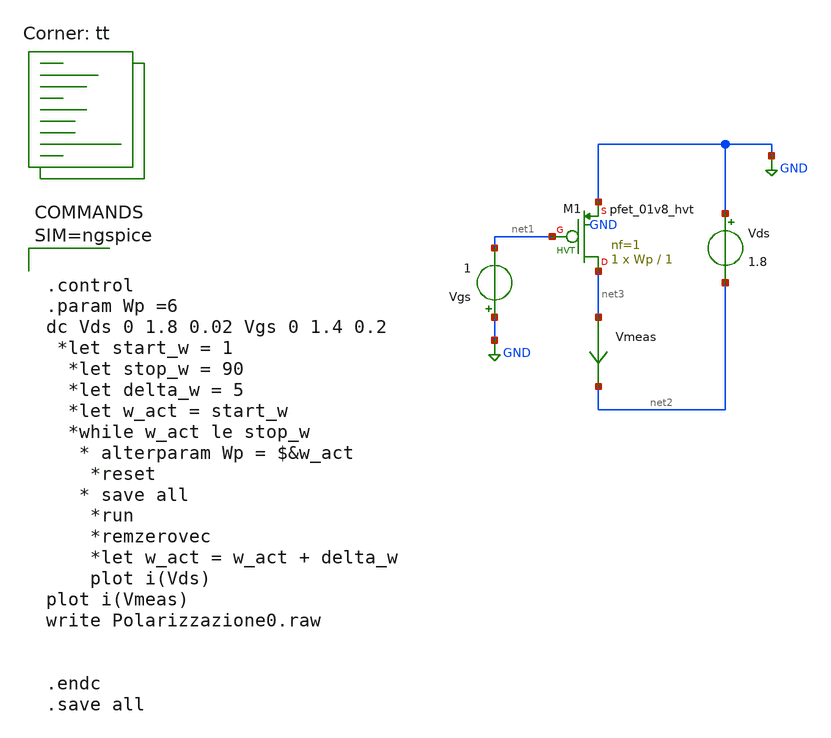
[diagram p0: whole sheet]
** sch_path: xschem/Polarizzazione0.sch
**.subckt Polarizzazione0
Vgs GND net1 1
Vds GND net2 1.8
XM1 net3 net1 GND GND sky130_fd_pr__pfet_01v8_hvt L=1 W=Wp nf=1 ad='int((nf+1)/2) * W/nf * 0.29' as='int((nf+2)/2) * W/nf * 0.29'
+ pd='2*int((nf+1)/2) * (W/nf + 0.29)' ps='2*int((nf+2)/2) * (W/nf + 0.29)' nrd='0.29 / W' nrs='0.29 / W'
+ sa=0 sb=0 sd=0 mult=1 m=1
Vmeas net3 net2 0
.save i(vmeas)
**** begin user architecture code
.lib $::SKYWATER_MODELS/sky130.lib.spice tt



.control
.param Wp =6
dc Vds 0 1.8 0.02 Vgs 0 1.4 0.2
 *let start_w = 1
  *let stop_w = 90
  *let delta_w = 5
  *let w_act = start_w
  *while w_act le stop_w
   * alterparam Wp = $&w_act
    *reset
   * save all
    *run
    *remzerovec
    *let w_act = w_act + delta_w
    plot i(Vds)
plot i(Vmeas)
write Polarizzazione0.raw


.endc
.save all




**** end user architecture code
**.ends
.GLOBAL GND
.end
